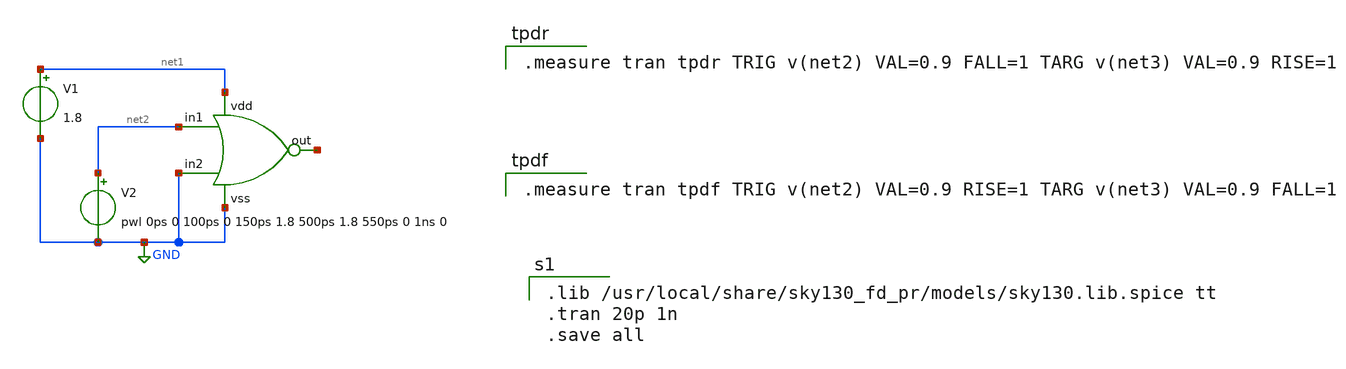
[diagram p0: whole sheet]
** sch_path: projects/carry_lookahead_adder/xschem/ports/test/rise_fall_time/_xor.sch
**.subckt _xor
V1 net1 GND 1.8
V2 net2 GND pwl 0ps 0 100ps 0 150ps 1.8 500ps 1.8 550ps 0 1ns 0
x1 net2 GND net3 net1 GND nor
**** begin user architecture code

.lib /usr/local/share/sky130_fd_pr/models/sky130.lib.spice tt
.tran 20p 1n
.save all


.measure tran tpdr TRIG v(net2) VAL=0.9 FALL=1 TARG v(net3) VAL=0.9 RISE=1


.measure tran tpdf TRIG v(net2) VAL=0.9 RISE=1 TARG v(net3) VAL=0.9 FALL=1

**** end user architecture code
**.ends

* expanding   symbol:  nor.sym # of pins=5
** sym_path: projects/carry_lookahead_adder/xschem/ports/nor.sym
** sch_path: projects/carry_lookahead_adder/xschem/ports/nor.sch
.subckt nor in1 in2 out vdd vss
*.ipin in1
*.ipin in2
*.opin out
*.ipin vdd
*.ipin vss
XM3 out in1 vss vss sky130_fd_pr__nfet_01v8 L=0.15 W=1 nf=1 ad='int((nf+1)/2) * W/nf * 0.29' as='int((nf+2)/2) * W/nf * 0.29'
+ pd='2*int((nf+1)/2) * (W/nf + 0.29)' ps='2*int((nf+2)/2) * (W/nf + 0.29)' nrd='0.29 / W' nrs='0.29 / W'
+ sa=0 sb=0 sd=0 mult=1 m=1
XM4 out in2 vss vss sky130_fd_pr__nfet_01v8 L=0.15 W=1 nf=1 ad='int((nf+1)/2) * W/nf * 0.29' as='int((nf+2)/2) * W/nf * 0.29'
+ pd='2*int((nf+1)/2) * (W/nf + 0.29)' ps='2*int((nf+2)/2) * (W/nf + 0.29)' nrd='0.29 / W' nrs='0.29 / W'
+ sa=0 sb=0 sd=0 mult=1 m=1
XM1 net1 in1 vdd net3 sky130_fd_pr__pfet_01v8 L=0.15 W=4.15 nf=1 ad='int((nf+1)/2) * W/nf * 0.29' as='int((nf+2)/2) * W/nf * 0.29'
+ pd='2*int((nf+1)/2) * (W/nf + 0.29)' ps='2*int((nf+2)/2) * (W/nf + 0.29)' nrd='0.29 / W' nrs='0.29 / W'
+ sa=0 sb=0 sd=0 mult=1 m=1
XM2 out in2 net1 net2 sky130_fd_pr__pfet_01v8 L=0.15 W=4.15 nf=1 ad='int((nf+1)/2) * W/nf * 0.29' as='int((nf+2)/2) * W/nf * 0.29'
+ pd='2*int((nf+1)/2) * (W/nf + 0.29)' ps='2*int((nf+2)/2) * (W/nf + 0.29)' nrd='0.29 / W' nrs='0.29 / W'
+ sa=0 sb=0 sd=0 mult=1 m=1
.ends

.GLOBAL GND
.end
